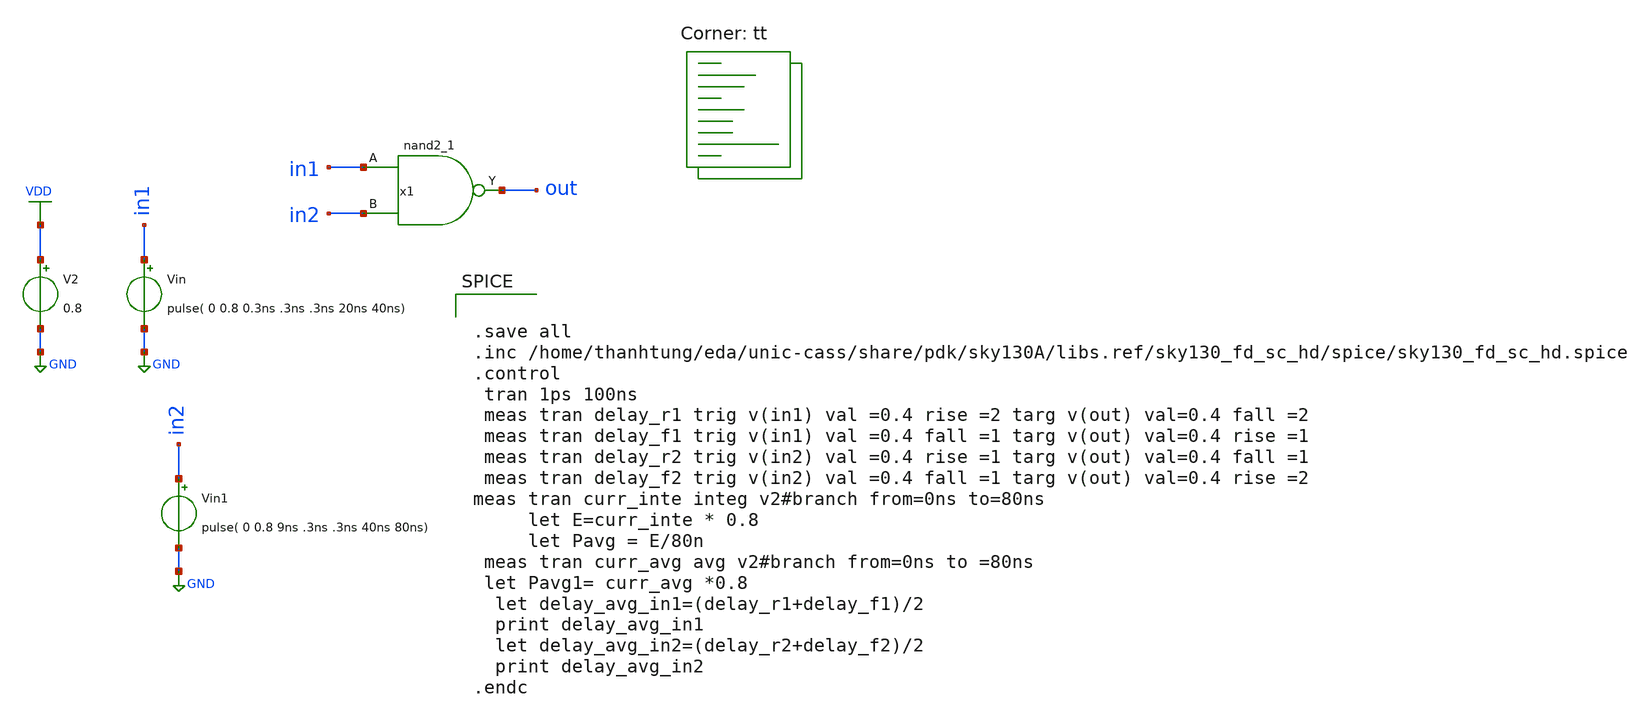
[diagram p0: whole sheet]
** sch_path: d_2nand_para.sch
**.subckt d_2nand_para
x1 in1 in2 GND GND VDD VDD out sky130_fd_sc_hd__nand2_1
V2 VDD GND 0.8
Vin in1 GND pulse( 0 0.8 0.3ns .3ns .3ns 20ns 40ns)
Vin1 in2 GND pulse( 0 0.8 9ns .3ns .3ns 40ns 80ns)
**** begin user architecture code


.save all
.inc /home/thanhtung/eda/unic-cass/share/pdk/sky130A/libs.ref/sky130_fd_sc_hd/spice/sky130_fd_sc_hd.spice
.control
 tran 1ps 100ns
 meas tran delay_r1 trig v(in1) val =0.4 rise =2 targ v(out) val=0.4 fall =2
 meas tran delay_f1 trig v(in1) val =0.4 fall =1 targ v(out) val=0.4 rise =1
 meas tran delay_r2 trig v(in2) val =0.4 rise =1 targ v(out) val=0.4 fall =1
 meas tran delay_f2 trig v(in2) val =0.4 fall =1 targ v(out) val=0.4 rise =2
meas tran curr_inte integ v2#branch from=0ns to=80ns
 	let E=curr_inte * 0.8
	 let Pavg = E/80n
 meas tran curr_avg avg v2#branch from=0ns to =80ns
 let Pavg1= curr_avg *0.8
  let delay_avg_in1=(delay_r1+delay_f1)/2
  print delay_avg_in1
  let delay_avg_in2=(delay_r2+delay_f2)/2
  print delay_avg_in2
.endc


.lib $::SKYWATER_MODELS/sky130.lib.spice tt
**** end user architecture code
**.ends
.GLOBAL GND
.GLOBAL VDD
.end
